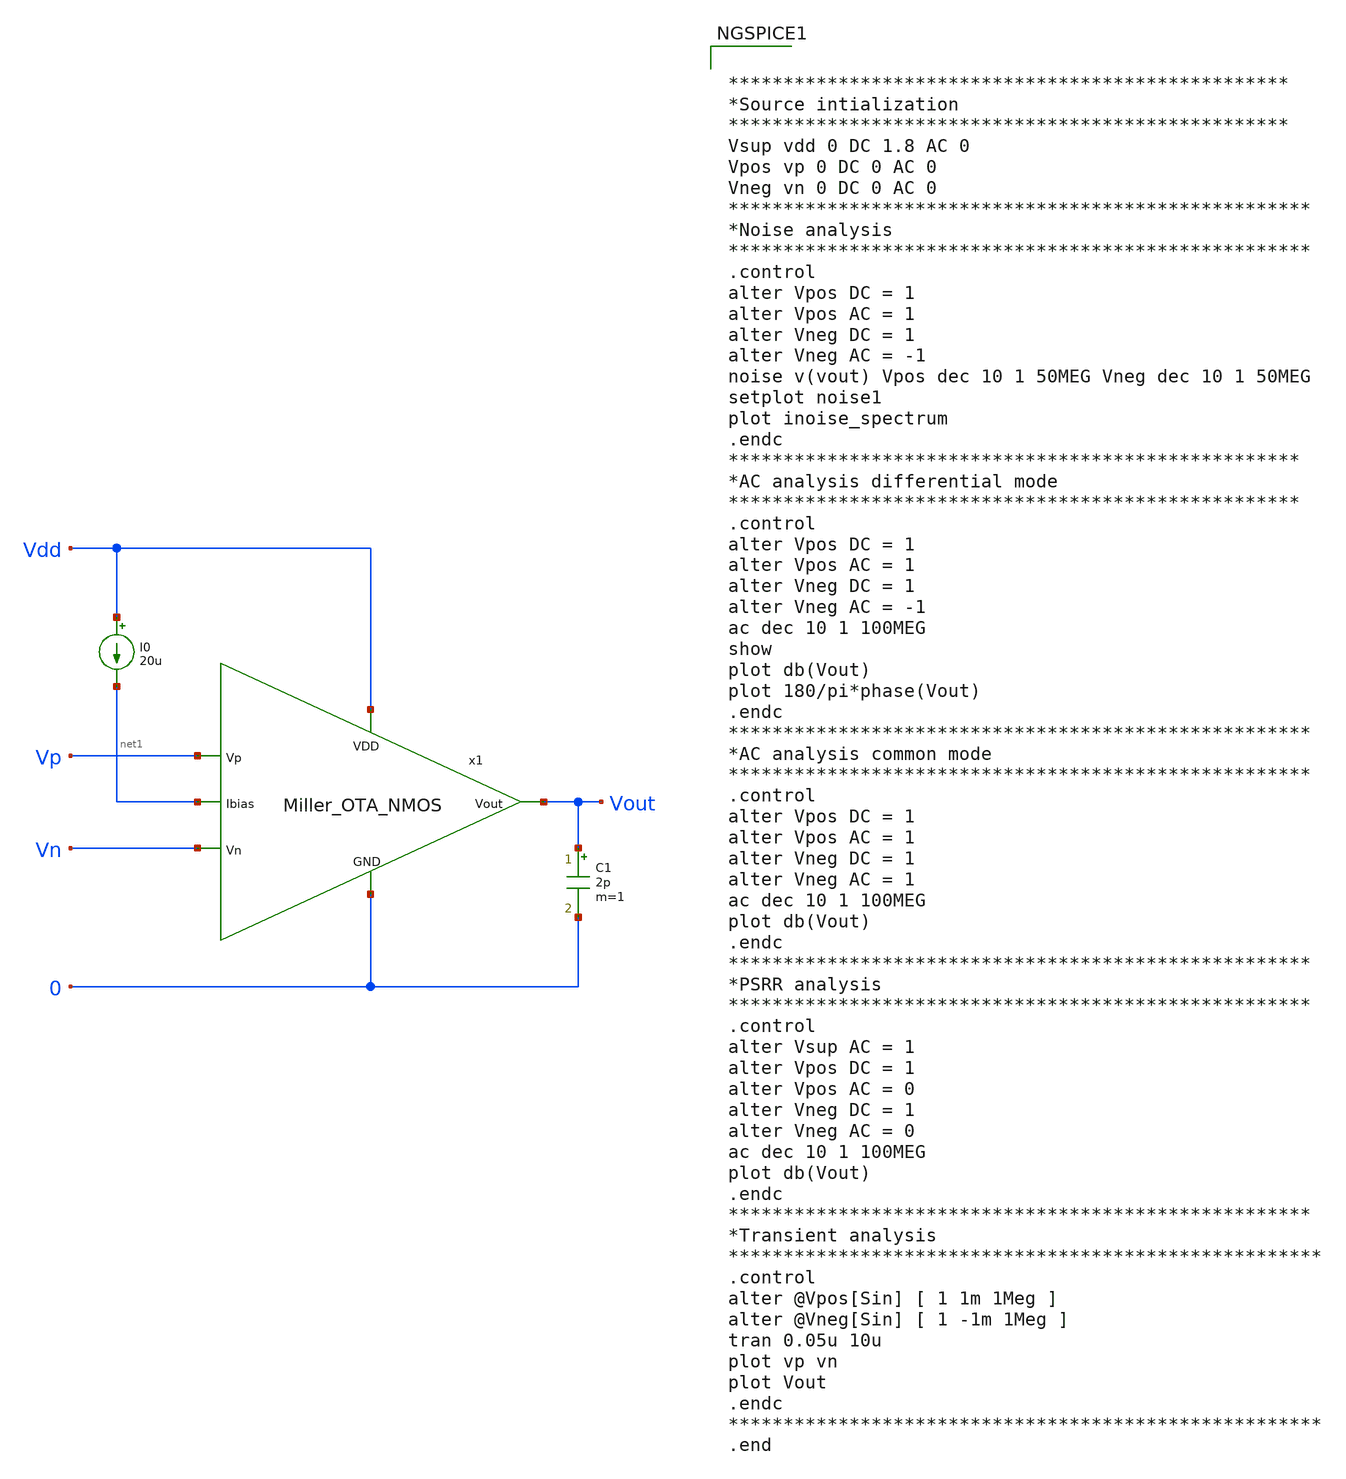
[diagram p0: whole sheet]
** sch_path: Analog_Blocks/OTA/Testbench/Miller_OTA_NMOS_TB.sch
**.subckt Miller_OTA_NMOS_TB
I0 Vdd net1 20u
C1 Vout 0 2p m=1
x1 Vdd Vn Vp Vout net1 0 Miller_OTA_NMOS
**** begin user architecture code


***************************************************
*Source intialization
***************************************************
Vsup vdd 0 DC 1.8 AC 0
Vpos vp 0 DC 0 AC 0
Vneg vn 0 DC 0 AC 0
*****************************************************
*Noise analysis
*****************************************************
.control
alter Vpos DC = 1
alter Vpos AC = 1
alter Vneg DC = 1
alter Vneg AC = -1
noise v(vout) Vpos dec 10 1 50MEG Vneg dec 10 1 50MEG
setplot noise1
plot inoise_spectrum
.endc
****************************************************
*AC analysis differential mode
****************************************************
.control
alter Vpos DC = 1
alter Vpos AC = 1
alter Vneg DC = 1
alter Vneg AC = -1
ac dec 10 1 100MEG
show
plot db(Vout)
plot 180/pi*phase(Vout)
.endc
*****************************************************
*AC analysis common mode
*****************************************************
.control
alter Vpos DC = 1
alter Vpos AC = 1
alter Vneg DC = 1
alter Vneg AC = 1
ac dec 10 1 100MEG
plot db(Vout)
.endc
*****************************************************
*PSRR analysis
*****************************************************
.control
alter Vsup AC = 1
alter Vpos DC = 1
alter Vpos AC = 0
alter Vneg DC = 1
alter Vneg AC = 0
ac dec 10 1 100MEG
plot db(Vout)
.endc
*****************************************************
*Transient analysis
******************************************************
.control
alter @Vpos[Sin] [ 1 1m 1Meg ]
alter @Vneg[Sin] [ 1 -1m 1Meg ]
tran 0.05u 10u
plot vp vn
plot Vout
.endc
******************************************************
.end



.include ~/Analog_blocks/models/skywater-pdk/libraries/sky130_fd_pr/latest/cells/nfet_01v8/sky130_fd_pr__nfet_01v8__tt.corner.spice
.include ~/Analog_blocks/models/skywater-pdk/libraries/sky130_fd_pr/latest/cells/nfet_01v8_lvt/sky130_fd_pr__nfet_01v8_lvt__tt.corner.spice
.include ~/Analog_blocks/models/skywater-pdk/libraries/sky130_fd_pr/latest/cells/pfet_01v8/sky130_fd_pr__pfet_01v8__tt.corner.spice
.include ~/Analog_blocks/models/skywater-pdk/libraries/sky130_fd_pr/latest/cells/nfet_03v3_nvt/sky130_fd_pr__nfet_03v3_nvt__tt.corner.spice
.include ~/Analog_blocks/models/skywater-pdk/libraries/sky130_fd_pr/latest/cells/nfet_05v0_nvt/sky130_fd_pr__nfet_05v0_nvt__tt.corner.spice
.include ~/Analog_blocks/models/skywater-pdk/libraries/sky130_fd_pr/latest/cells/esd_nfet_01v8/sky130_fd_pr__esd_nfet_01v8__tt.corner.spice
.include ~/Analog_blocks/models/skywater-pdk/libraries/sky130_fd_pr/latest/cells/pfet_01v8_lvt/sky130_fd_pr__pfet_01v8_lvt__tt.corner.spice
.include ~/Analog_blocks/models/skywater-pdk/libraries/sky130_fd_pr/latest/cells/pfet_01v8_hvt/sky130_fd_pr__pfet_01v8_hvt__tt.corner.spice
.include ~/Analog_blocks/models/skywater-pdk/libraries/sky130_fd_pr/latest/cells/esd_pfet_g5v0d10v5/sky130_fd_pr__esd_pfet_g5v0d10v5__tt.corner.spice
.include ~/Analog_blocks/models/skywater-pdk/libraries/sky130_fd_pr/latest/cells/pfet_g5v0d10v5/sky130_fd_pr__pfet_g5v0d10v5__tt.corner.spice
.include ~/Analog_blocks/models/skywater-pdk/libraries/sky130_fd_pr/latest/cells/pfet_g5v0d16v0/sky130_fd_pr__pfet_g5v0d16v0__tt.corner.spice
.include ~/Analog_blocks/models/skywater-pdk/libraries/sky130_fd_pr/latest/cells/nfet_g5v0d10v5/sky130_fd_pr__nfet_g5v0d10v5__tt.corner.spice
.include ~/Analog_blocks/models/skywater-pdk/libraries/sky130_fd_pr/latest/cells/nfet_g5v0d16v0/sky130_fd_pr__nfet_g5v0d16v0__tt_discrete.corner.spice
.include ~/Analog_blocks/models/skywater-pdk/libraries/sky130_fd_pr/latest/cells/esd_nfet_g5v0d10v5/sky130_fd_pr__esd_nfet_g5v0d10v5__tt.corner.spice
.include ~/Analog_blocks/models/skywater-pdk/libraries/sky130_fd_pr/latest/models/corners/tt/nonfet.spice
* Mismatch parameters
.include ~/Analog_blocks/models/skywater-pdk/libraries/sky130_fd_pr/latest/cells/nfet_01v8/sky130_fd_pr__nfet_01v8__mismatch.corner.spice
.include ~/Analog_blocks/models/skywater-pdk/libraries/sky130_fd_pr/latest/cells/pfet_01v8/sky130_fd_pr__pfet_01v8__mismatch.corner.spice
.include ~/Analog_blocks/models/skywater-pdk/libraries/sky130_fd_pr/latest/cells/nfet_01v8_lvt/sky130_fd_pr__nfet_01v8_lvt__mismatch.corner.spice
.include ~/Analog_blocks/models/skywater-pdk/libraries/sky130_fd_pr/latest/cells/pfet_01v8_lvt/sky130_fd_pr__pfet_01v8_lvt__mismatch.corner.spice
.include ~/Analog_blocks/models/skywater-pdk/libraries/sky130_fd_pr/latest/cells/pfet_01v8_hvt/sky130_fd_pr__pfet_01v8_hvt__mismatch.corner.spice
.include ~/Analog_blocks/models/skywater-pdk/libraries/sky130_fd_pr/latest/cells/nfet_g5v0d10v5/sky130_fd_pr__nfet_g5v0d10v5__mismatch.corner.spice
.include ~/Analog_blocks/models/skywater-pdk/libraries/sky130_fd_pr/latest/cells/pfet_g5v0d10v5/sky130_fd_pr__pfet_g5v0d10v5__mismatch.corner.spice
.include ~/Analog_blocks/models/skywater-pdk/libraries/sky130_fd_pr/latest/cells/nfet_05v0_nvt/sky130_fd_pr__nfet_05v0_nvt__mismatch.corner.spice
.include ~/Analog_blocks/models/skywater-pdk/libraries/sky130_fd_pr/latest/cells/nfet_03v3_nvt/sky130_fd_pr__nfet_03v3_nvt__mismatch.corner.spice
* Resistor
.include ~/Analog_blocks/models/skywater-pdk/libraries/sky130_fd_pr/latest/models/r+c/res_typical__cap_typical.spice
.include ~/Analog_blocks/models/skywater-pdk/libraries/sky130_fd_pr/latest/models/r+c/res_typical__cap_typical__lin.spice
* Special cells
.include ~/Analog_blocks/models/skywater-pdk/libraries/sky130_fd_pr/latest/models/corners/tt/specialized_cells.spice
* All models
.include ~/Analog_blocks/models/skywater-pdk/libraries/sky130_fd_pr/latest/models/all.spice
* Corner
.include ~/Analog_blocks/models/skywater-pdk/libraries/sky130_fd_pr/latest/models/corners/tt/rf.spice

**** end user architecture code
**.ends

* expanding   symbol:
*+  /home/eslam/Analog_blocks/Analog_Blocks/OTA/Schematic/Miller_OTA/Transistor5v/Miller_OTA_NMOS.sym # of pins=6
** sym_path: Analog_Blocks/OTA/Schematic/Miller_OTA/Transistor5v/Miller_OTA_NMOS.sym
** sch_path: Analog_Blocks/OTA/Schematic/Miller_OTA/Transistor5v/Miller_OTA_NMOS.sch
.subckt Miller_OTA_NMOS VDD Vn Vp Vout Ibias GND
*.ipin VDD
*.ipin Ibias
*.ipin Vn
*.ipin Vp
*.opin Vout
*.ipin GND
XM1 net1 Vn net3 GND sky130_fd_pr__nfet_g5v0d10v5 L=0.5 W=10 nf=1 ad='int((nf+1)/2) * W/nf * 0.29' as='int((nf+2)/2) * W/nf * 0.29'
+ pd='2*int((nf+1)/2) * (W/nf + 0.29)' ps='2*int((nf+2)/2) * (W/nf + 0.29)' nrd='0.29 / W' nrs='0.29 / W'
+ sa=0 sb=0 sd=0 mult=1 m=1
XM2 net2 Vp net3 GND sky130_fd_pr__nfet_g5v0d10v5 L=0.5 W=10 nf=1 ad='int((nf+1)/2) * W/nf * 0.29' as='int((nf+2)/2) * W/nf * 0.29'
+ pd='2*int((nf+1)/2) * (W/nf + 0.29)' ps='2*int((nf+2)/2) * (W/nf + 0.29)' nrd='0.29 / W' nrs='0.29 / W'
+ sa=0 sb=0 sd=0 mult=1 m=1
XM3 net1 net1 VDD VDD sky130_fd_pr__pfet_g5v0d10v5 L=0.5 W=20 nf=1 ad='int((nf+1)/2) * W/nf * 0.29' as='int((nf+2)/2) * W/nf * 0.29'
+ pd='2*int((nf+1)/2) * (W/nf + 0.29)' ps='2*int((nf+2)/2) * (W/nf + 0.29)' nrd='0.29 / W' nrs='0.29 / W'
+ sa=0 sb=0 sd=0 mult=5 m=5
XM4 net2 net1 VDD VDD sky130_fd_pr__pfet_g5v0d10v5 L=0.5 W=20 nf=1 ad='int((nf+1)/2) * W/nf * 0.29' as='int((nf+2)/2) * W/nf * 0.29'
+ pd='2*int((nf+1)/2) * (W/nf + 0.29)' ps='2*int((nf+2)/2) * (W/nf + 0.29)' nrd='0.29 / W' nrs='0.29 / W'
+ sa=0 sb=0 sd=0 mult=5 m=5
XM6 Vout net2 VDD VDD sky130_fd_pr__pfet_g5v0d10v5 L=0.5 W=20 nf=1 ad='int((nf+1)/2) * W/nf * 0.29' as='int((nf+2)/2) * W/nf * 0.29'
+ pd='2*int((nf+1)/2) * (W/nf + 0.29)' ps='2*int((nf+2)/2) * (W/nf + 0.29)' nrd='0.29 / W' nrs='0.29 / W'
+ sa=0 sb=0 sd=0 mult=20 m=20
XM5 net3 Ibias GND GND sky130_fd_pr__nfet_g5v0d10v5 L=1 W=3 nf=1 ad='int((nf+1)/2) * W/nf * 0.29' as='int((nf+2)/2) * W/nf * 0.29'
+ pd='2*int((nf+1)/2) * (W/nf + 0.29)' ps='2*int((nf+2)/2) * (W/nf + 0.29)' nrd='0.29 / W' nrs='0.29 / W'
+ sa=0 sb=0 sd=0 mult=8 m=8
XM8 Ibias Ibias GND GND sky130_fd_pr__nfet_g5v0d10v5 L=1 W=3 nf=1 ad='int((nf+1)/2) * W/nf * 0.29' as='int((nf+2)/2) * W/nf * 0.29'
+ pd='2*int((nf+1)/2) * (W/nf + 0.29)' ps='2*int((nf+2)/2) * (W/nf + 0.29)' nrd='0.29 / W' nrs='0.29 / W'
+ sa=0 sb=0 sd=0 mult=8 m=8
XC1 net2 Vout sky130_fd_pr__cap_mim_m3_2 W=1 L=1 MF=1 m=1
XM7 Vout Ibias GND GND sky130_fd_pr__nfet_g5v0d10v5 L=1 W=3 nf=1 ad='int((nf+1)/2) * W/nf * 0.29' as='int((nf+2)/2) * W/nf * 0.29'
+ pd='2*int((nf+1)/2) * (W/nf + 0.29)' ps='2*int((nf+2)/2) * (W/nf + 0.29)' nrd='0.29 / W' nrs='0.29 / W'
+ sa=0 sb=0 sd=0 mult=16 m=16
.ends

.end
